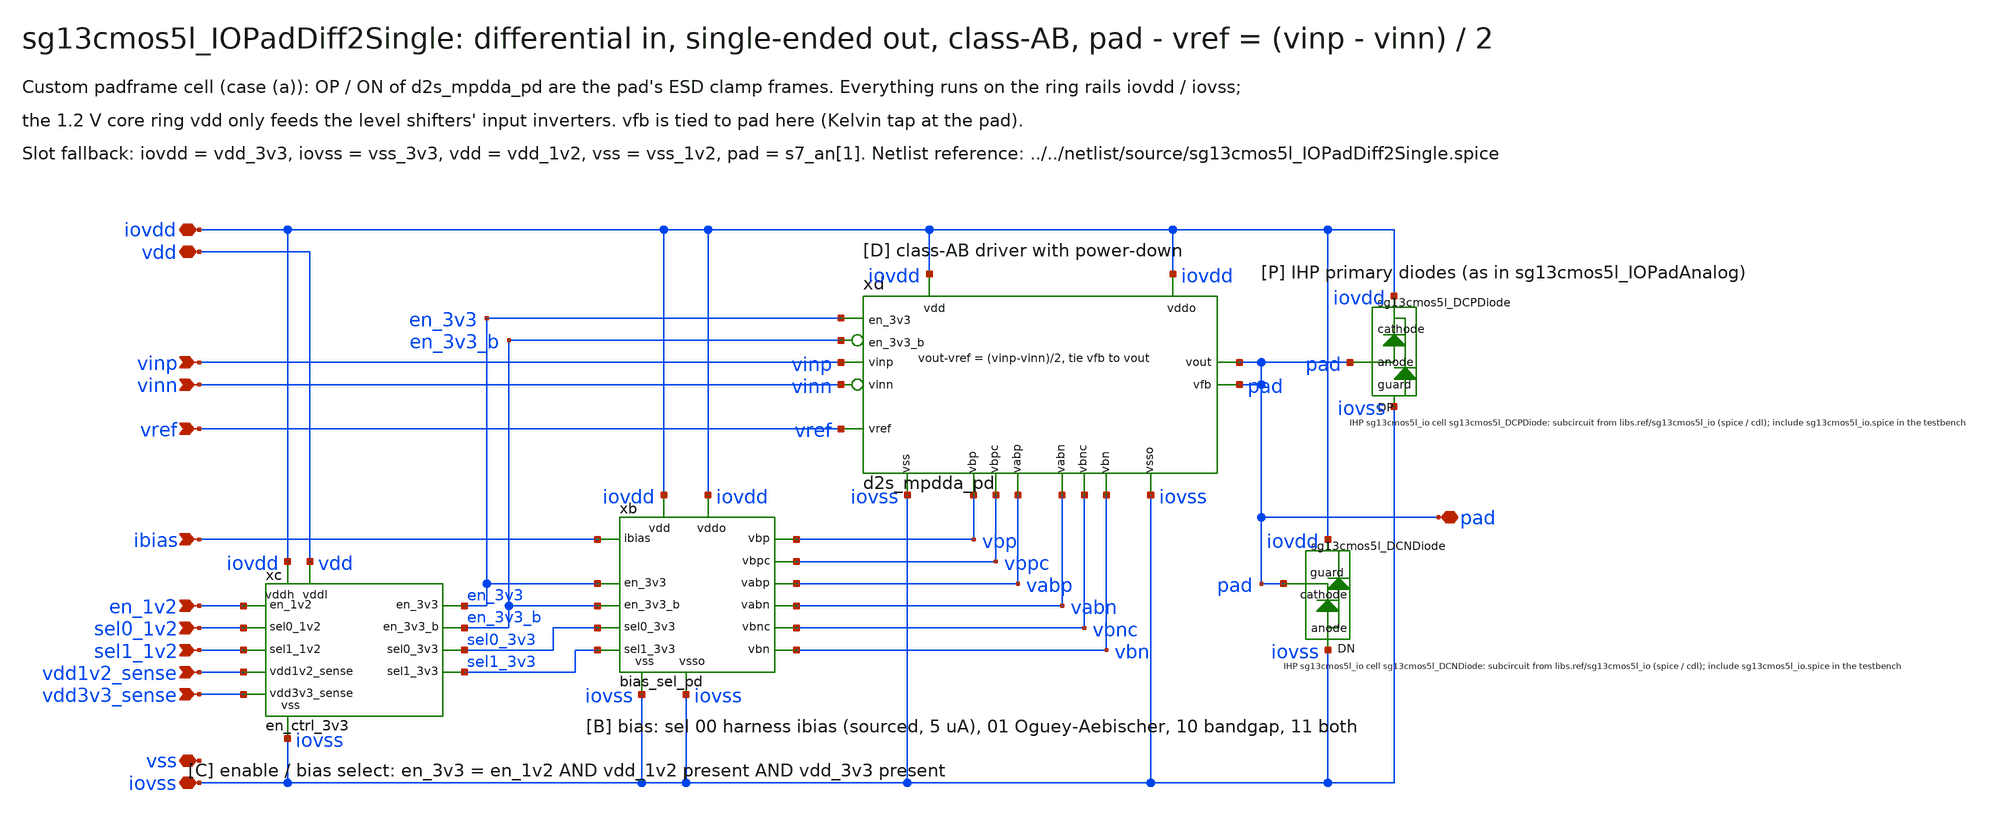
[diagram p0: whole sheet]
** sch_path: sudelbuecher/design_considerations/consolidation/ab_regroup_2026-10-28/before/macros/sg13cmos5l_IOPadDiff2Single/schematic/xschem/sg13cmos5l_IOPadDiff2Single.sch
**.subckt sg13cmos5l_IOPadDiff2Single iovdd iovss vdd vss pad vinp vinn vref ibias en_1v2 sel0_1v2
*+ sel1_1v2 vdd1v2_sense vdd3v3_sense
*.iopin iovdd
*.iopin iovss
*.iopin vdd
*.iopin vss
*.iopin pad
*.ipin vinp
*.ipin vinn
*.ipin vref
*.ipin ibias
*.ipin en_1v2
*.ipin sel0_1v2
*.ipin sel1_1v2
*.ipin vdd1v2_sense
*.ipin vdd3v3_sense
xc iovdd vdd iovss en_1v2 sel0_1v2 sel1_1v2 vdd1v2_sense vdd3v3_sense en_3v3 sel0_3v3 sel1_3v3
+ en_3v3_b en_ctrl_3v3
xb iovdd iovss iovdd iovss ibias vbp vbn vbpc vbnc vabp vabn en_3v3 sel0_3v3 sel1_3v3 en_3v3_b
+ bias_sel_pd
xd iovdd iovss iovdd iovss vinp vinn vref pad pad vbp vbn vbpc vbnc vabp vabn en_3v3 en_3v3_b
+ d2s_mpdda_pd
XDN iovss pad iovdd sg13cmos5l_DCNDiode
XDP pad iovdd iovss sg13cmos5l_DCPDiode
**.ends
.end
